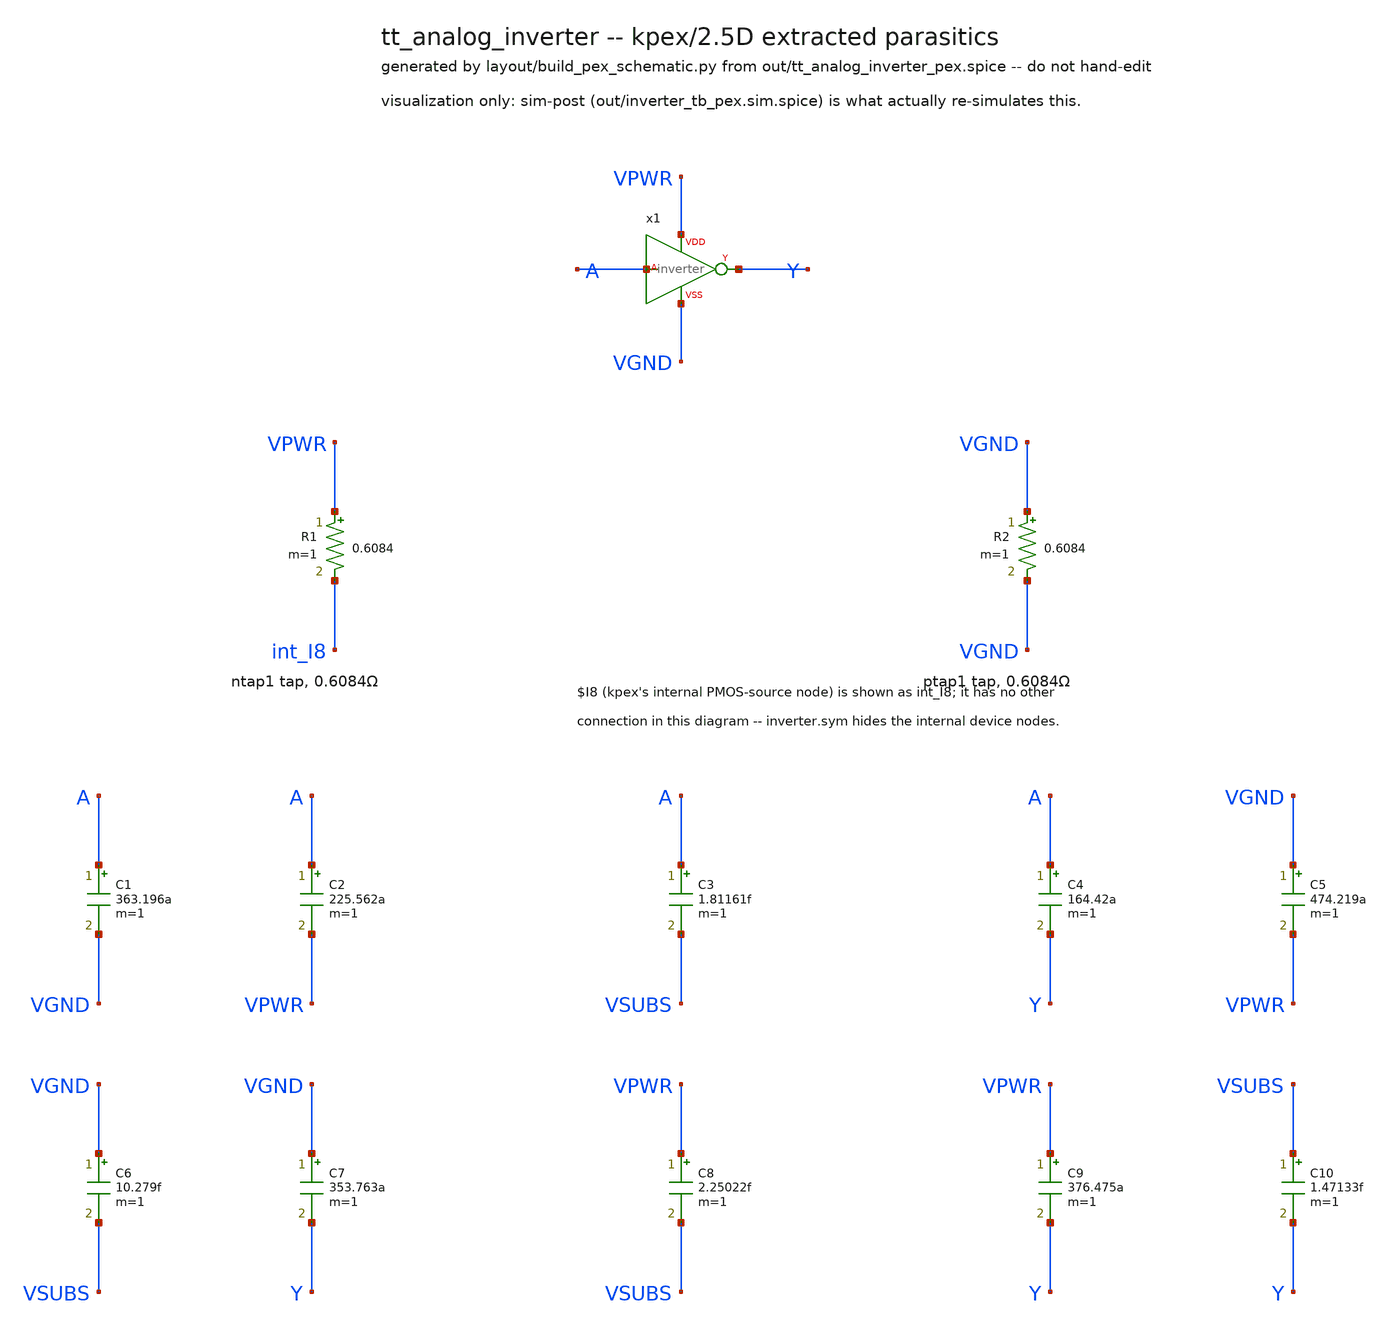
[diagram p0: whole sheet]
** sch_path: analog/xschem/tt_analog_inverter_pex_viz.sch
**.subckt tt_analog_inverter_pex_viz
x1 A Y VPWR VGND inverter
R1 VPWR int_I8 0.6084 m=1
R2 VGND VGND 0.6084 m=1
C1 A VGND 363.196a m=1
C2 A VPWR 225.562a m=1
C3 A VSUBS 1.81161f m=1
C4 A Y 164.42a m=1
C5 VGND VPWR 474.219a m=1
C6 VGND VSUBS 10.279f m=1
C7 VGND Y 353.763a m=1
C8 VPWR VSUBS 2.25022f m=1
C9 VPWR Y 376.475a m=1
C10 VSUBS Y 1.47133f m=1
**.ends

* expanding   symbol:  /work/analog/xschem/inverter.sym # of pins=4
** sym_path: analog/xschem/inverter.sym
** sch_path: analog/xschem/inverter.sch
.subckt inverter A Y VDD VSS
*.ipin A
*.opin Y
*.iopin VDD
*.iopin VSS
XM1 Y A VDD VDD sg13_lv_pmos w=2.0u l=0.13u ng=1 m=1 mm_ok=1
XM2 Y A VSS VSS sg13_lv_nmos w=1.0u l=0.13u ng=1 m=1 mm_ok=1
.ends

.end
